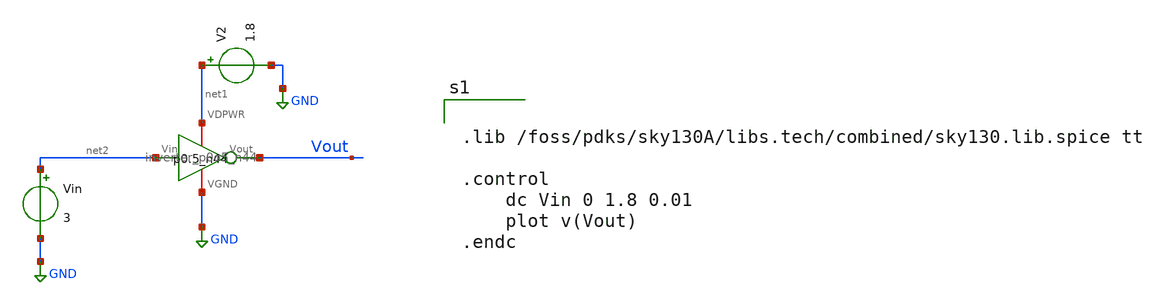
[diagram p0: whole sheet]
** sch_path: tt_um_emmersonv_tiq_adc/xschem/unit_inverter_test.sch
**.subckt unit_inverter_test
Vin net2 GND 3
V2 net1 GND 1.8
x1 net1 Vout net2 GND inverter_p0o5_n44
**** begin user architecture code


.lib /foss/pdks/sky130A/libs.tech/combined/sky130.lib.spice tt

.control
	dc Vin 0 1.8 0.01
	plot v(Vout)
.endc


**** end user architecture code
**.ends
.GLOBAL GND
.end
